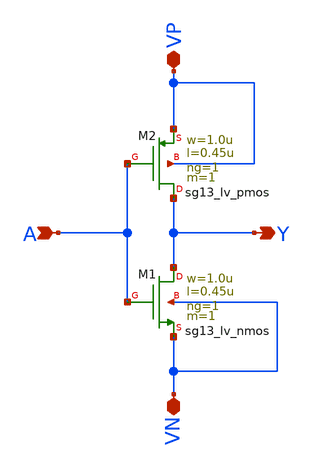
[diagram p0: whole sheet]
** sch_path: Team 2 Design/design_data/t2_inverter.sch
**.subckt t2_inverter VP VN A Y
*.iopin VP
*.iopin VN
*.ipin A
*.opin Y
XM2 Y A VP VP sg13_lv_pmos w=1.0u l=0.45u ng=1 m=1 mm_ok=1
XM1 Y A VN VN sg13_lv_nmos w=1.0u l=0.45u ng=1 m=1 mm_ok=1
**.ends
.end
